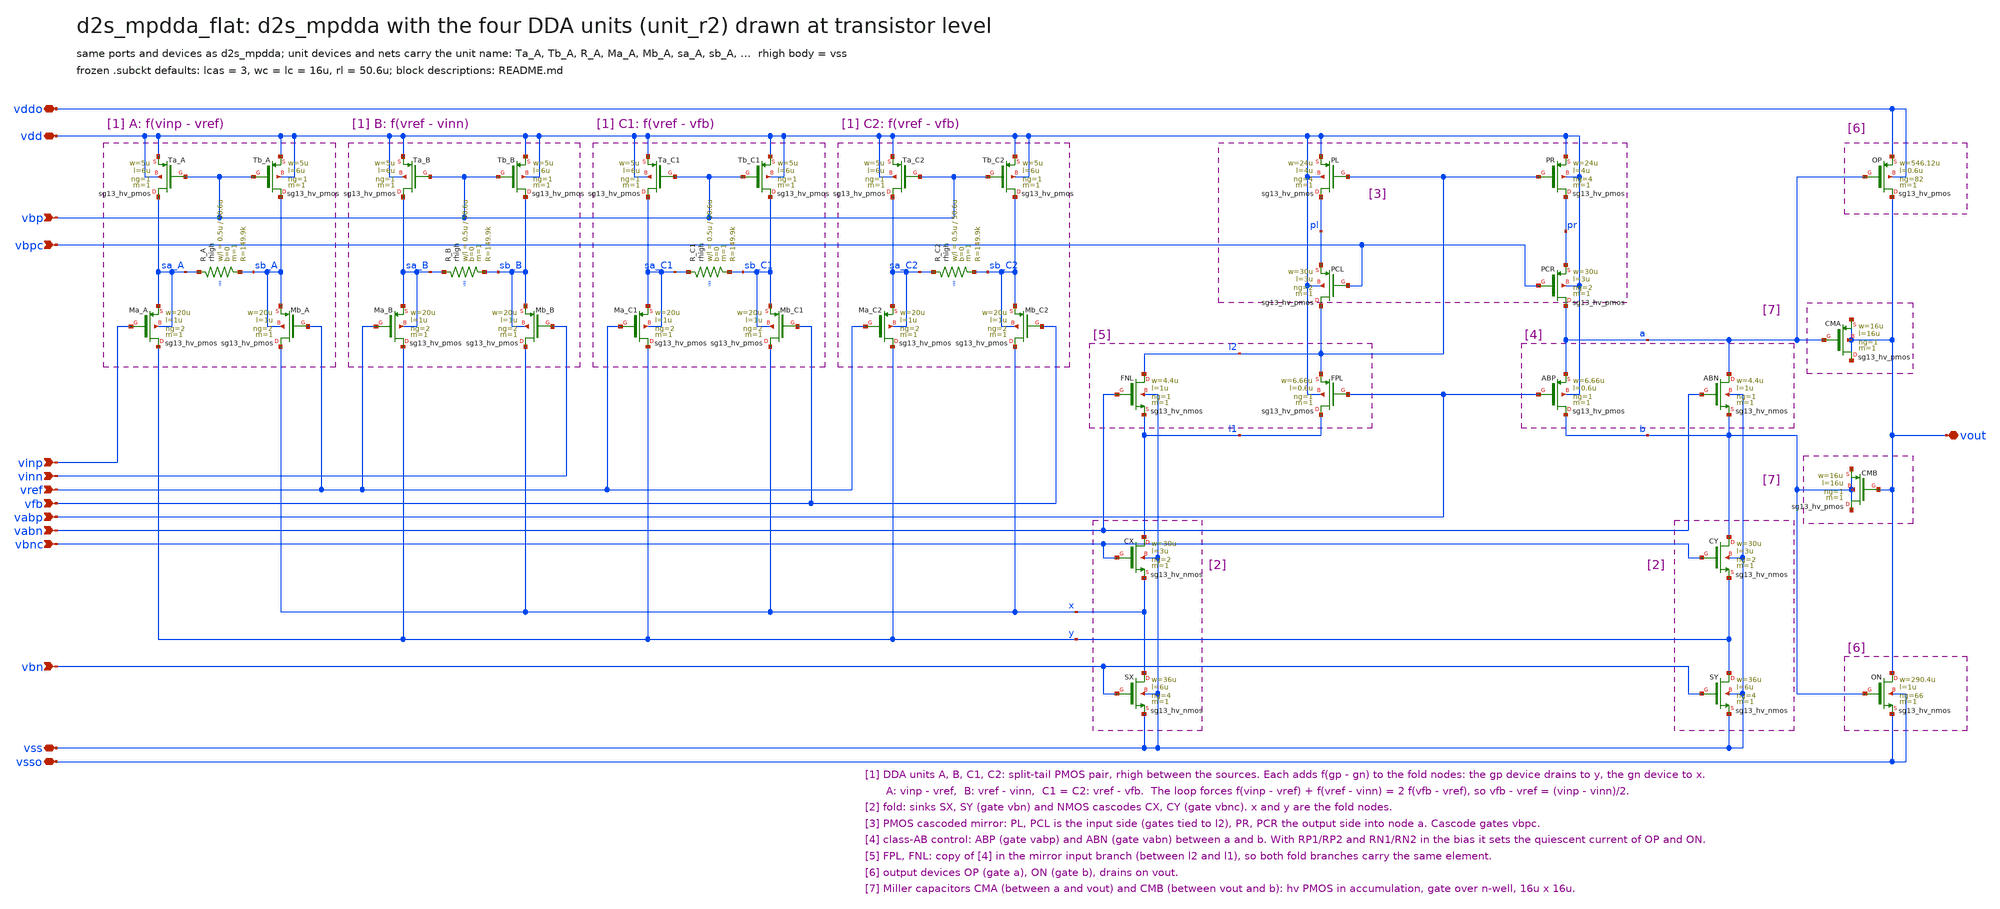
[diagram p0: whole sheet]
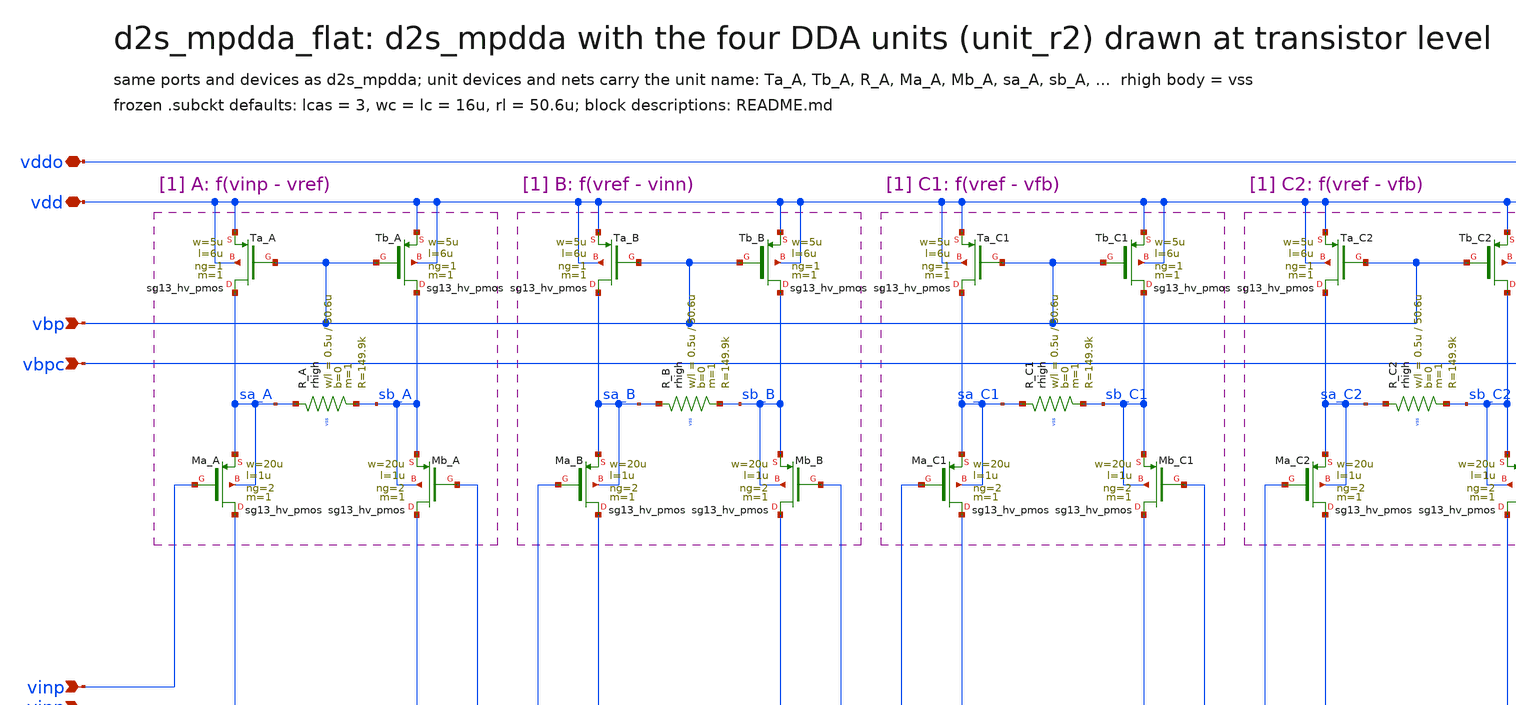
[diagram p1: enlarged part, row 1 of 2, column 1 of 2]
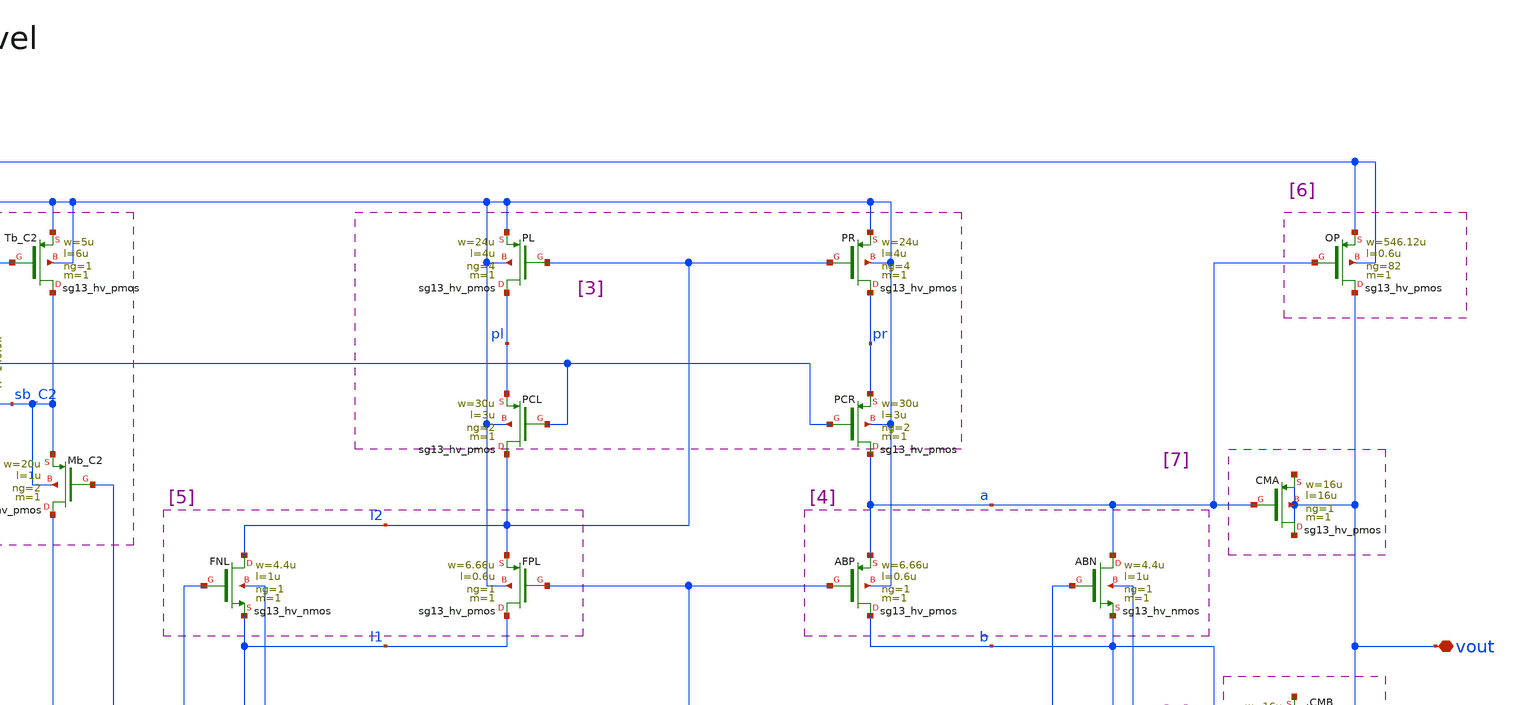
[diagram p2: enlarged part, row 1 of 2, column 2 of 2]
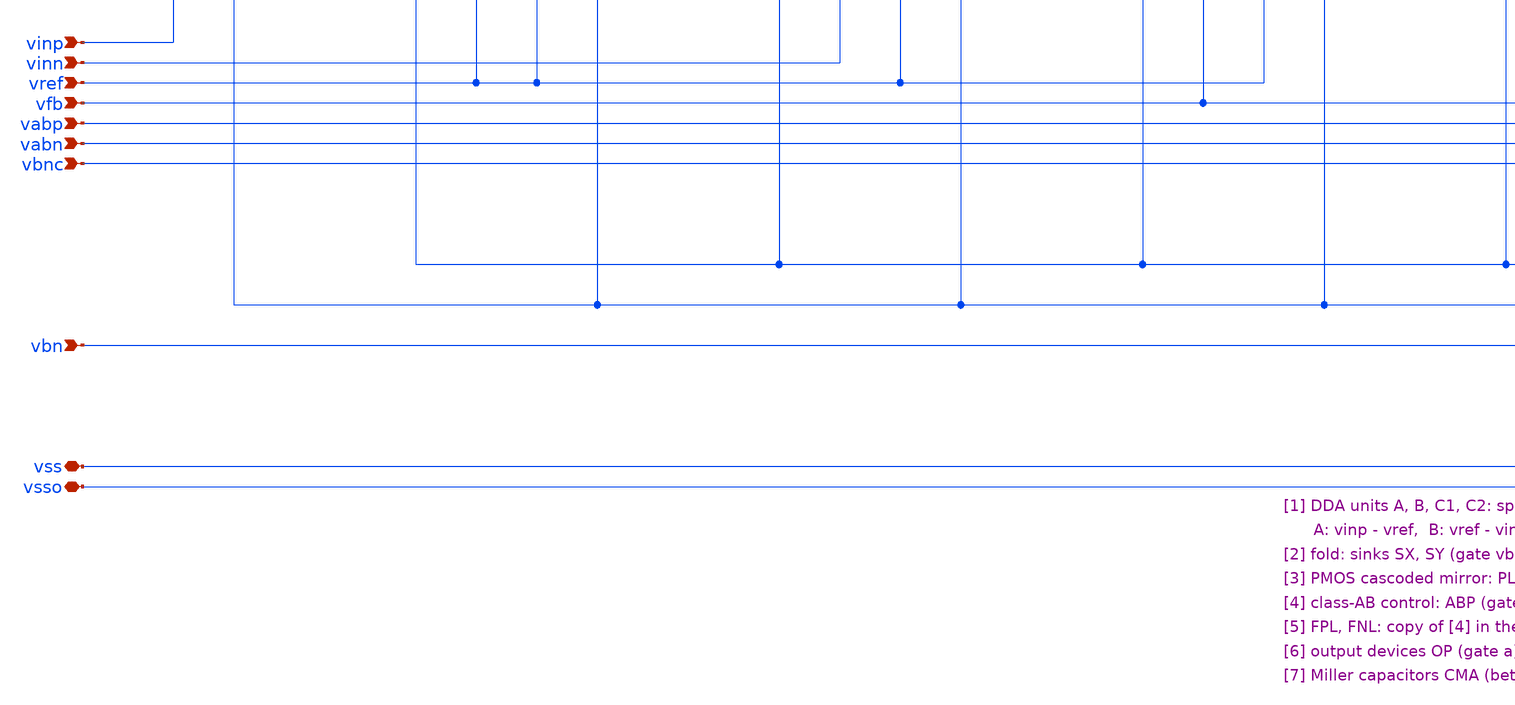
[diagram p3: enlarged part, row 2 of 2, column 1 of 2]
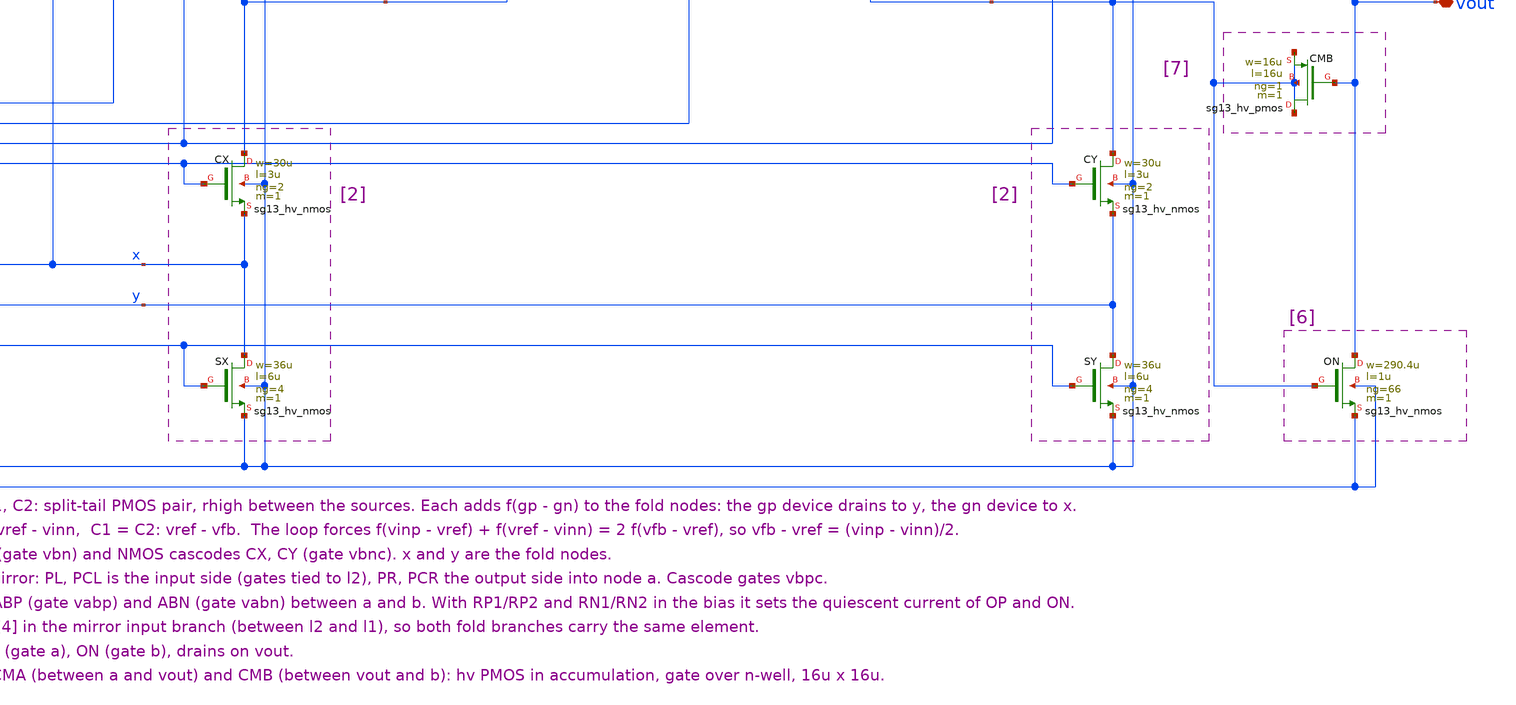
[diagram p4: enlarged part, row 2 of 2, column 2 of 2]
** sch_path: sudelbuecher/design_considerations/class_ab_pad_driver/improvements/xschem/d2s_mpdda_flat.sch
**.subckt d2s_mpdda_flat vdd vss vddo vsso vinp vinn vref vout vfb vbp vbn vbpc vbnc vabp vabn
*.iopin vdd
*.iopin vss
*.iopin vddo
*.iopin vsso
*.ipin vinp
*.ipin vinn
*.ipin vref
*.iopin vout
*.ipin vfb
*.ipin vbp
*.ipin vbn
*.ipin vbpc
*.ipin vbnc
*.ipin vabp
*.ipin vabn
XTa_A sa_A vbp vdd vdd sg13_hv_pmos w=5u l=6u ng=1 m=1 mm_ok=1
XTb_A sb_A vbp vdd vdd sg13_hv_pmos w=5u l=6u ng=1 m=1 mm_ok=1
XR_A sa_A sb_A vss rhigh w=0.5u l=50.6u m=1 b=0 mm_ok=1
XMa_A y vinp sa_A sa_A sg13_hv_pmos w=20u l=1u ng=2 m=1 mm_ok=1
XMb_A x vref sb_A sb_A sg13_hv_pmos w=20u l=1u ng=2 m=1 mm_ok=1
XTa_B sa_B vbp vdd vdd sg13_hv_pmos w=5u l=6u ng=1 m=1 mm_ok=1
XTb_B sb_B vbp vdd vdd sg13_hv_pmos w=5u l=6u ng=1 m=1 mm_ok=1
XR_B sa_B sb_B vss rhigh w=0.5u l=50.6u m=1 b=0 mm_ok=1
XMa_B y vref sa_B sa_B sg13_hv_pmos w=20u l=1u ng=2 m=1 mm_ok=1
XMb_B x vinn sb_B sb_B sg13_hv_pmos w=20u l=1u ng=2 m=1 mm_ok=1
XTa_C1 sa_C1 vbp vdd vdd sg13_hv_pmos w=5u l=6u ng=1 m=1 mm_ok=1
XTb_C1 sb_C1 vbp vdd vdd sg13_hv_pmos w=5u l=6u ng=1 m=1 mm_ok=1
XR_C1 sa_C1 sb_C1 vss rhigh w=0.5u l=50.6u m=1 b=0 mm_ok=1
XMa_C1 y vref sa_C1 sa_C1 sg13_hv_pmos w=20u l=1u ng=2 m=1 mm_ok=1
XMb_C1 x vfb sb_C1 sb_C1 sg13_hv_pmos w=20u l=1u ng=2 m=1 mm_ok=1
XTa_C2 sa_C2 vbp vdd vdd sg13_hv_pmos w=5u l=6u ng=1 m=1 mm_ok=1
XTb_C2 sb_C2 vbp vdd vdd sg13_hv_pmos w=5u l=6u ng=1 m=1 mm_ok=1
XR_C2 sa_C2 sb_C2 vss rhigh w=0.5u l=50.6u m=1 b=0 mm_ok=1
XMa_C2 y vref sa_C2 sa_C2 sg13_hv_pmos w=20u l=1u ng=2 m=1 mm_ok=1
XMb_C2 x vfb sb_C2 sb_C2 sg13_hv_pmos w=20u l=1u ng=2 m=1 mm_ok=1
XFNL l2 vabn l1 vss sg13_hv_nmos w=4.4u l=1u ng=1 m=1 mm_ok=1
XCX l1 vbnc x vss sg13_hv_nmos w=30u l=3u ng=2 m=1 mm_ok=1
XSX x vbn vss vss sg13_hv_nmos w=36u l=6u ng=4 m=1 mm_ok=1
XPL pl l2 vdd vdd sg13_hv_pmos w=24u l=4u ng=4 m=1 mm_ok=1
XPCL l2 vbpc pl vdd sg13_hv_pmos w=30u l=3u ng=2 m=1 mm_ok=1
XFPL l1 vabp l2 vdd sg13_hv_pmos w=6.66u l=0.6u ng=1 m=1 mm_ok=1
XPR pr l2 vdd vdd sg13_hv_pmos w=24u l=4u ng=4 m=1 mm_ok=1
XPCR a vbpc pr vdd sg13_hv_pmos w=30u l=3u ng=2 m=1 mm_ok=1
XABP b vabp a vdd sg13_hv_pmos w=6.66u l=0.6u ng=1 m=1 mm_ok=1
XABN a vabn b vss sg13_hv_nmos w=4.4u l=1u ng=1 m=1 mm_ok=1
XCY b vbnc y vss sg13_hv_nmos w=30u l=3u ng=2 m=1 mm_ok=1
XSY y vbn vss vss sg13_hv_nmos w=36u l=6u ng=4 m=1 mm_ok=1
XOP vout a vddo vddo sg13_hv_pmos w=546.12u l=0.6u ng=82 m=1 mm_ok=1
XON vout b vsso vsso sg13_hv_nmos w=290.4u l=1u ng=66 m=1 mm_ok=1
XCMA vout a vout vout sg13_hv_pmos w=16u l=16u ng=1 m=1 mm_ok=1
XCMB b vout b b sg13_hv_pmos w=16u l=16u ng=1 m=1 mm_ok=1
**.ends
.end
